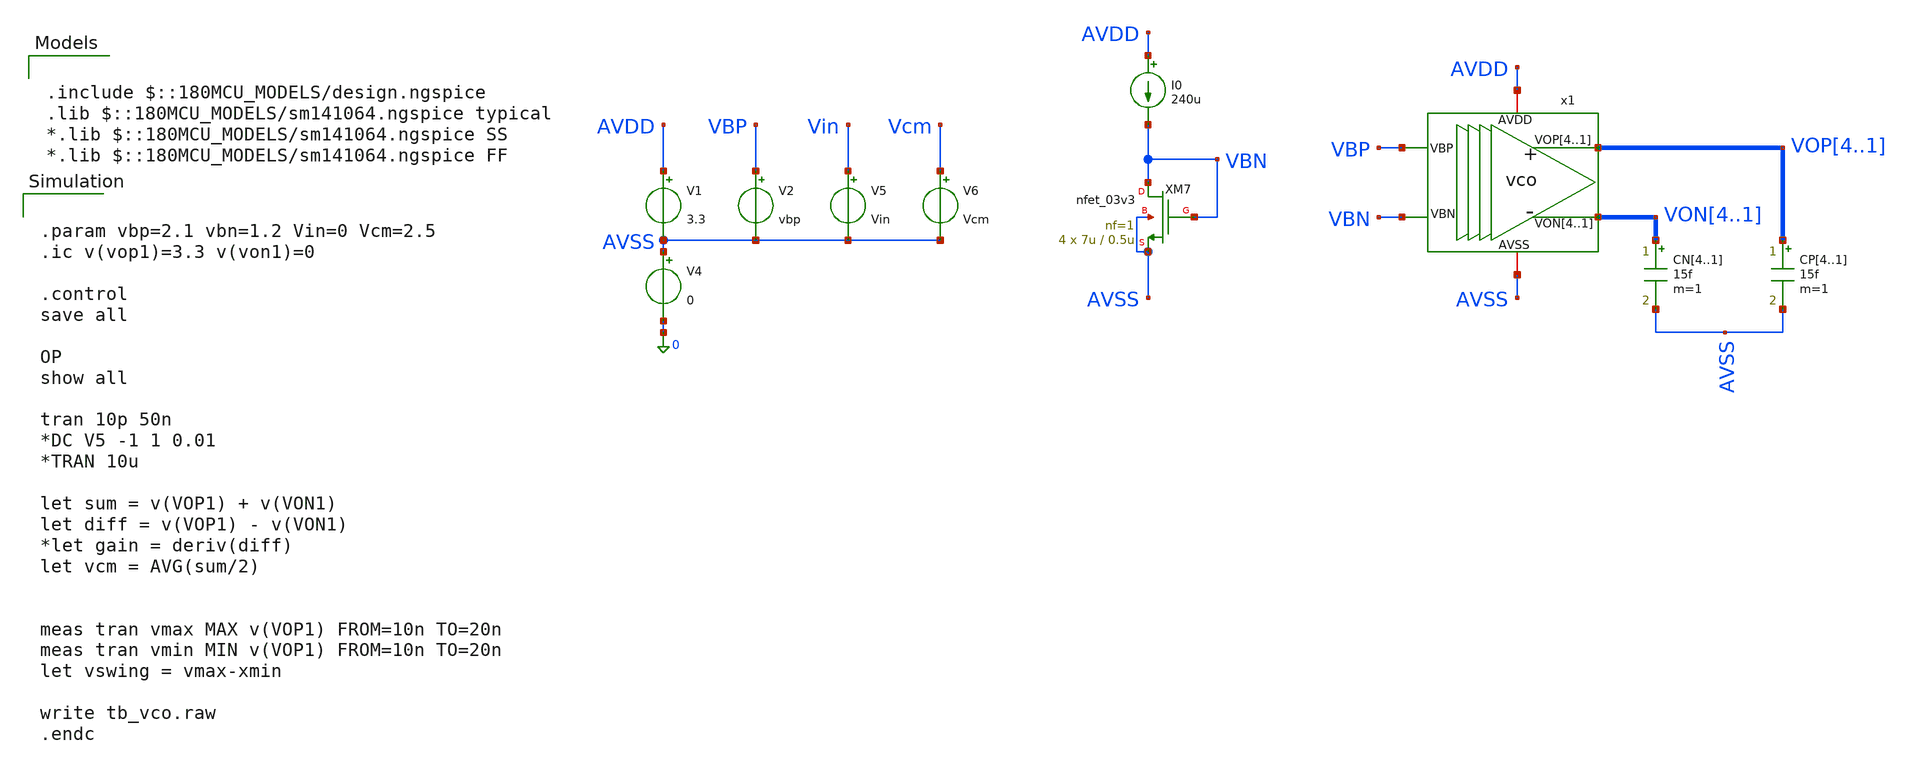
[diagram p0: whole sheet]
** sch_path: designs/libs/tb_analog/tb_vco/tb_vco.sch
**.subckt tb_vco
x1 VOP4 VOP3 VOP2 VOP1 VON4 VON3 VON2 VON1 AVDD AVSS VBP VBN vco
V1 AVDD AVSS 3.3
V2 VBP AVSS vbp
V4 AVSS 0 0
V5 Vin AVSS Vin
V6 Vcm AVSS Vcm
CP4 VOP4 AVSS 15f m=1
CP3 VOP3 AVSS 15f m=1
CP2 VOP2 AVSS 15f m=1
CP1 VOP1 AVSS 15f m=1
CN4 VON4 AVSS 15f m=1
CN3 VON3 AVSS 15f m=1
CN2 VON2 AVSS 15f m=1
CN1 VON1 AVSS 15f m=1
XM7 VBN VBN AVSS AVSS nfet_03v3 L=0.5u W=7u nf=1 ad='int((nf+1)/2) * W/nf * 0.18u' as='int((nf+2)/2) * W/nf * 0.18u'
+ pd='2*int((nf+1)/2) * (W/nf + 0.18u)' ps='2*int((nf+2)/2) * (W/nf + 0.18u)' nrd='0.18u / W' nrs='0.18u / W'
+ sa=0 sb=0 sd=0 m=4
I0 AVDD VBN 240u
**** begin user architecture code


.param vbp=2.1 vbn=1.2 Vin=0 Vcm=2.5
.ic v(vop1)=3.3 v(von1)=0

.control
save all

OP
show all

tran 10p 50n
*DC V5 -1 1 0.01
*TRAN 10u

let sum = v(VOP1) + v(VON1)
let diff = v(VOP1) - v(VON1)
*let gain = deriv(diff)
let vcm = AVG(sum/2)


meas tran vmax MAX v(VOP1) FROM=10n TO=20n
meas tran vmin MIN v(VOP1) FROM=10n TO=20n
let vswing = vmax-xmin

write tb_vco.raw
.endc



.include $::180MCU_MODELS/design.ngspice
.lib $::180MCU_MODELS/sm141064.ngspice typical
*.lib $::180MCU_MODELS/sm141064.ngspice SS
*.lib $::180MCU_MODELS/sm141064.ngspice FF

**** end user architecture code
**.ends

* expanding   symbol:  libs/core_analog/vco/vco.sym # of pins=6
** sym_path: designs/libs/core_analog/vco/vco.sym
** sch_path: designs/libs/core_analog/vco/vco.sch
.subckt vco VOP4 VOP3 VOP2 VOP1 VON4 VON3 VON2 VON1 AVDD AVSS VBP VBN
*.opin VOP4,VOP3,VOP2,VOP1
*.opin VON4,VON3,VON2,VON1
*.ipin VBP
*.ipin VBN
*.iopin AVDD
*.iopin AVSS
x1 VOP1 AVDD VOP4 VON4 VON1 AVSS VBP VBN delay_stage
x2 VOP2 AVDD VON1 VOP1 VON2 AVSS VBP VBN delay_stage
x3 VOP3 AVDD VON2 VOP2 VON3 AVSS VBP VBN delay_stage
x4 VOP4 AVDD VON3 VOP3 VON4 AVSS VBP VBN delay_stage
.ends


* expanding   symbol:  libs/core_analog/delay_stage/delay_stage.sym # of pins=8
** sym_path: designs/libs/core_analog/delay_stage/delay_stage.sym
** sch_path: designs/libs/core_analog/delay_stage/delay_stage.sch
.subckt delay_stage VOP AVDD VIP VIN VON AVSS VBP VBN
*.ipin VIP
*.ipin VIN
*.opin VOP
*.opin VON
*.iopin AVDD
*.iopin AVSS
*.ipin VBP
*.ipin VBN
XM5 VON VIP net1 AVSS nfet_03v3 L=0.5u W=2.08u nf=1 ad='int((nf+1)/2) * W/nf * 0.18u' as='int((nf+2)/2) * W/nf * 0.18u'
+ pd='2*int((nf+1)/2) * (W/nf + 0.18u)' ps='2*int((nf+2)/2) * (W/nf + 0.18u)' nrd='0.18u / W' nrs='0.18u / W'
+ sa=0 sb=0 sd=0 m=8
XM2 VON VON AVDD AVDD pfet_03v3 L=1.5u W=1.1u nf=1 ad='int((nf+1)/2) * W/nf * 0.18u' as='int((nf+2)/2) * W/nf * 0.18u'
+ pd='2*int((nf+1)/2) * (W/nf + 0.18u)' ps='2*int((nf+2)/2) * (W/nf + 0.18u)' nrd='0.18u / W' nrs='0.18u / W'
+ sa=0 sb=0 sd=0 m=8
XM6 VOP VIN net1 AVSS nfet_03v3 L=0.5u W=2.08u nf=1 ad='int((nf+1)/2) * W/nf * 0.18u' as='int((nf+2)/2) * W/nf * 0.18u'
+ pd='2*int((nf+1)/2) * (W/nf + 0.18u)' ps='2*int((nf+2)/2) * (W/nf + 0.18u)' nrd='0.18u / W' nrs='0.18u / W'
+ sa=0 sb=0 sd=0 m=8
XM1 VON VBP AVDD AVDD pfet_03v3 L=1.5u W=1.1u nf=1 ad='int((nf+1)/2) * W/nf * 0.18u' as='int((nf+2)/2) * W/nf * 0.18u'
+ pd='2*int((nf+1)/2) * (W/nf + 0.18u)' ps='2*int((nf+2)/2) * (W/nf + 0.18u)' nrd='0.18u / W' nrs='0.18u / W'
+ sa=0 sb=0 sd=0 m=8
XM3 VOP VBP AVDD AVDD pfet_03v3 L=1.5u W=1.1u nf=1 ad='int((nf+1)/2) * W/nf * 0.18u' as='int((nf+2)/2) * W/nf * 0.18u'
+ pd='2*int((nf+1)/2) * (W/nf + 0.18u)' ps='2*int((nf+2)/2) * (W/nf + 0.18u)' nrd='0.18u / W' nrs='0.18u / W'
+ sa=0 sb=0 sd=0 m=8
XM4 VOP VOP AVDD AVDD pfet_03v3 L=1.5u W=1.1u nf=1 ad='int((nf+1)/2) * W/nf * 0.18u' as='int((nf+2)/2) * W/nf * 0.18u'
+ pd='2*int((nf+1)/2) * (W/nf + 0.18u)' ps='2*int((nf+2)/2) * (W/nf + 0.18u)' nrd='0.18u / W' nrs='0.18u / W'
+ sa=0 sb=0 sd=0 m=8
XM8 net1 VBN AVSS AVSS nfet_03v3 L=0.5u W=11.25u nf=1 ad='int((nf+1)/2) * W/nf * 0.18u' as='int((nf+2)/2) * W/nf * 0.18u'
+ pd='2*int((nf+1)/2) * (W/nf + 0.18u)' ps='2*int((nf+2)/2) * (W/nf + 0.18u)' nrd='0.18u / W' nrs='0.18u / W'
+ sa=0 sb=0 sd=0 m=8
.ends

.end
